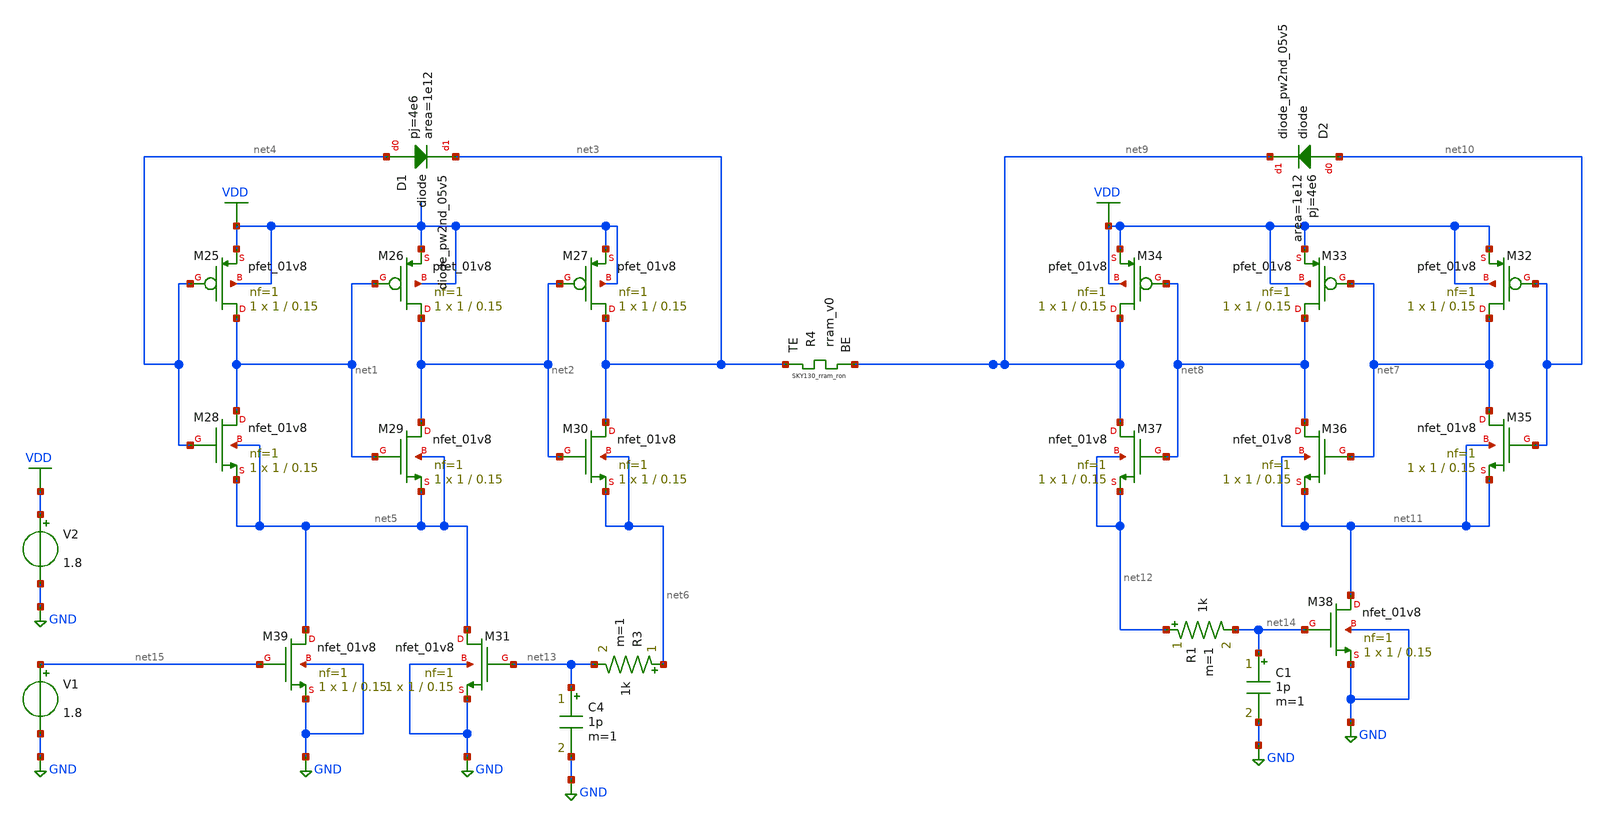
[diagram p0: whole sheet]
** sch_path: voltage_controlled_oscillator/vc_oscillator_tb.sch
**.subckt vc_oscillator_tb
XM25 net1 net4 VDD VDD sky130_fd_pr__pfet_01v8 L=0.15 W=1 nf=1 ad='int((nf+1)/2) * W/nf * 0.29' as='int((nf+2)/2) * W/nf * 0.29'
+ pd='2*int((nf+1)/2) * (W/nf + 0.29)' ps='2*int((nf+2)/2) * (W/nf + 0.29)' nrd='0.29 / W' nrs='0.29 / W'
+ sa=0 sb=0 sd=0 mult=1 m=1
XM26 net2 net1 VDD VDD sky130_fd_pr__pfet_01v8 L=0.15 W=1 nf=1 ad='int((nf+1)/2) * W/nf * 0.29' as='int((nf+2)/2) * W/nf * 0.29'
+ pd='2*int((nf+1)/2) * (W/nf + 0.29)' ps='2*int((nf+2)/2) * (W/nf + 0.29)' nrd='0.29 / W' nrs='0.29 / W'
+ sa=0 sb=0 sd=0 mult=1 m=1
XM27 net3 net2 VDD VDD sky130_fd_pr__pfet_01v8 L=0.15 W=1 nf=1 ad='int((nf+1)/2) * W/nf * 0.29' as='int((nf+2)/2) * W/nf * 0.29'
+ pd='2*int((nf+1)/2) * (W/nf + 0.29)' ps='2*int((nf+2)/2) * (W/nf + 0.29)' nrd='0.29 / W' nrs='0.29 / W'
+ sa=0 sb=0 sd=0 mult=1 m=1
XM28 net1 net4 net5 net5 sky130_fd_pr__nfet_01v8 L=0.15 W=1 nf=1 ad='int((nf+1)/2) * W/nf * 0.29' as='int((nf+2)/2) * W/nf * 0.29'
+ pd='2*int((nf+1)/2) * (W/nf + 0.29)' ps='2*int((nf+2)/2) * (W/nf + 0.29)' nrd='0.29 / W' nrs='0.29 / W'
+ sa=0 sb=0 sd=0 mult=1 m=1
XM29 net2 net1 net5 net5 sky130_fd_pr__nfet_01v8 L=0.15 W=1 nf=1 ad='int((nf+1)/2) * W/nf * 0.29' as='int((nf+2)/2) * W/nf * 0.29'
+ pd='2*int((nf+1)/2) * (W/nf + 0.29)' ps='2*int((nf+2)/2) * (W/nf + 0.29)' nrd='0.29 / W' nrs='0.29 / W'
+ sa=0 sb=0 sd=0 mult=1 m=1
XM30 net3 net2 net6 net6 sky130_fd_pr__nfet_01v8 L=0.15 W=1 nf=1 ad='int((nf+1)/2) * W/nf * 0.29' as='int((nf+2)/2) * W/nf * 0.29'
+ pd='2*int((nf+1)/2) * (W/nf + 0.29)' ps='2*int((nf+2)/2) * (W/nf + 0.29)' nrd='0.29 / W' nrs='0.29 / W'
+ sa=0 sb=0 sd=0 mult=1 m=1
XM31 net5 net13 GND GND sky130_fd_pr__nfet_01v8 L=0.15 W=1 nf=1 ad='int((nf+1)/2) * W/nf * 0.29' as='int((nf+2)/2) * W/nf * 0.29'
+ pd='2*int((nf+1)/2) * (W/nf + 0.29)' ps='2*int((nf+2)/2) * (W/nf + 0.29)' nrd='0.29 / W' nrs='0.29 / W'
+ sa=0 sb=0 sd=0 mult=1 m=1
XM32 net7 net10 VDD VDD sky130_fd_pr__pfet_01v8 L=0.15 W=1 nf=1 ad='int((nf+1)/2) * W/nf * 0.29' as='int((nf+2)/2) * W/nf * 0.29'
+ pd='2*int((nf+1)/2) * (W/nf + 0.29)' ps='2*int((nf+2)/2) * (W/nf + 0.29)' nrd='0.29 / W' nrs='0.29 / W'
+ sa=0 sb=0 sd=0 mult=1 m=1
XM33 net8 net7 VDD VDD sky130_fd_pr__pfet_01v8 L=0.15 W=1 nf=1 ad='int((nf+1)/2) * W/nf * 0.29' as='int((nf+2)/2) * W/nf * 0.29'
+ pd='2*int((nf+1)/2) * (W/nf + 0.29)' ps='2*int((nf+2)/2) * (W/nf + 0.29)' nrd='0.29 / W' nrs='0.29 / W'
+ sa=0 sb=0 sd=0 mult=1 m=1
XM34 net9 net8 VDD VDD sky130_fd_pr__pfet_01v8 L=0.15 W=1 nf=1 ad='int((nf+1)/2) * W/nf * 0.29' as='int((nf+2)/2) * W/nf * 0.29'
+ pd='2*int((nf+1)/2) * (W/nf + 0.29)' ps='2*int((nf+2)/2) * (W/nf + 0.29)' nrd='0.29 / W' nrs='0.29 / W'
+ sa=0 sb=0 sd=0 mult=1 m=1
XM35 net7 net10 net11 net11 sky130_fd_pr__nfet_01v8 L=0.15 W=1 nf=1 ad='int((nf+1)/2) * W/nf * 0.29'
+ as='int((nf+2)/2) * W/nf * 0.29' pd='2*int((nf+1)/2) * (W/nf + 0.29)' ps='2*int((nf+2)/2) * (W/nf + 0.29)'
+ nrd='0.29 / W' nrs='0.29 / W' sa=0 sb=0 sd=0 mult=1 m=1
XM36 net8 net7 net11 net11 sky130_fd_pr__nfet_01v8 L=0.15 W=1 nf=1 ad='int((nf+1)/2) * W/nf * 0.29' as='int((nf+2)/2) * W/nf * 0.29'
+ pd='2*int((nf+1)/2) * (W/nf + 0.29)' ps='2*int((nf+2)/2) * (W/nf + 0.29)' nrd='0.29 / W' nrs='0.29 / W'
+ sa=0 sb=0 sd=0 mult=1 m=1
XM37 net9 net8 net12 net12 sky130_fd_pr__nfet_01v8 L=0.15 W=1 nf=1 ad='int((nf+1)/2) * W/nf * 0.29' as='int((nf+2)/2) * W/nf * 0.29'
+ pd='2*int((nf+1)/2) * (W/nf + 0.29)' ps='2*int((nf+2)/2) * (W/nf + 0.29)' nrd='0.29 / W' nrs='0.29 / W'
+ sa=0 sb=0 sd=0 mult=1 m=1
XM38 net11 net14 GND GND sky130_fd_pr__nfet_01v8 L=0.15 W=1 nf=1 ad='int((nf+1)/2) * W/nf * 0.29' as='int((nf+2)/2) * W/nf * 0.29'
+ pd='2*int((nf+1)/2) * (W/nf + 0.29)' ps='2*int((nf+2)/2) * (W/nf + 0.29)' nrd='0.29 / W' nrs='0.29 / W'
+ sa=0 sb=0 sd=0 mult=1 m=1
XR4 net3 net9 rram_v0
XM39 net5 net15 GND GND sky130_fd_pr__nfet_01v8 L=0.15 W=1 nf=1 ad='int((nf+1)/2) * W/nf * 0.29' as='int((nf+2)/2) * W/nf * 0.29'
+ pd='2*int((nf+1)/2) * (W/nf + 0.29)' ps='2*int((nf+2)/2) * (W/nf + 0.29)' nrd='0.29 / W' nrs='0.29 / W'
+ sa=0 sb=0 sd=0 mult=1 m=1
XD1 net4 net3 sky130_fd_pr__diode_pw2nd_05v5 area=1e12 pj=4e6
XD2 net10 net9 sky130_fd_pr__diode_pw2nd_05v5 area=1e12 pj=4e6
R3 net6 net13 1k m=1
C4 net13 GND 1p m=1
R1 net12 net14 1k m=1
C1 net14 GND 1p m=1
V1 net15 GND 1.8
.save i(v1)
V2 VDD GND 1.8
.save i(v2)
**.ends
.GLOBAL GND
.GLOBAL VDD
.end
